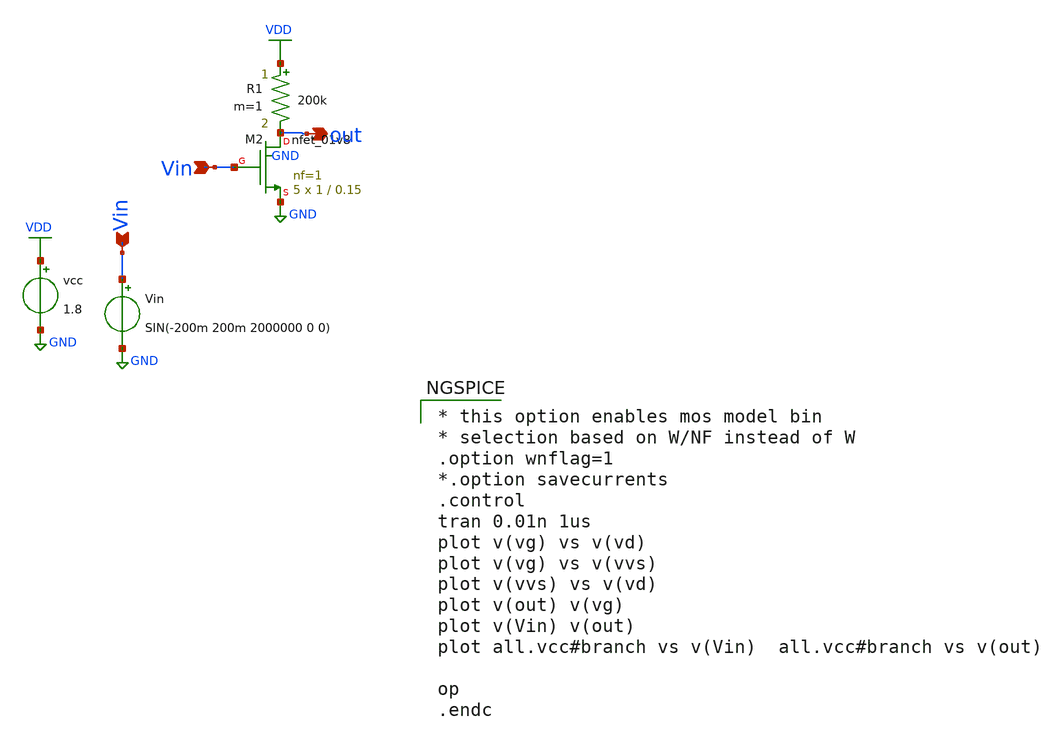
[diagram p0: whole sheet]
** sch_path: xschem/untitled-1.sch
**.subckt untitled-1 Vin Vin out
*.ipin Vin
*.ipin Vin
*.opin out
XM2 out Vin GND GND sky130_fd_pr__nfet_01v8 L=0.15 W=1 nf=1 ad='int((nf+1)/2) * W/nf * 0.29' as='int((nf+2)/2) * W/nf * 0.29'
+ pd='2*int((nf+1)/2) * (W/nf + 0.29)' ps='2*int((nf+2)/2) * (W/nf + 0.29)' nrd='0.29 / W' nrs='0.29 / W'
+ sa=0 sb=0 sd=0 mult=5 m=5
Vin Vin GND SIN(-200m 200m 2000000 0 0)
vcc VDD GND 1.8
R1 VDD out 200k m=1
**** begin user architecture code

* this option enables mos model bin
* selection based on W/NF instead of W
.option wnflag=1
*.option savecurrents
.control
tran 0.01n 1us
plot v(vg) vs v(vd)
plot v(vg) vs v(vvs)
plot v(vvs) vs v(vd)
plot v(out) v(vg)
plot v(Vin) v(out)
plot all.vcc#branch vs v(Vin)  all.vcc#branch vs v(out)

op
.endc



** opencircuitdesign pdks install
.lib $::SKYWATER_MODELS/sky130.lib.spice tt


**** end user architecture code
**.ends
.GLOBAL GND
.GLOBAL VDD
.end
